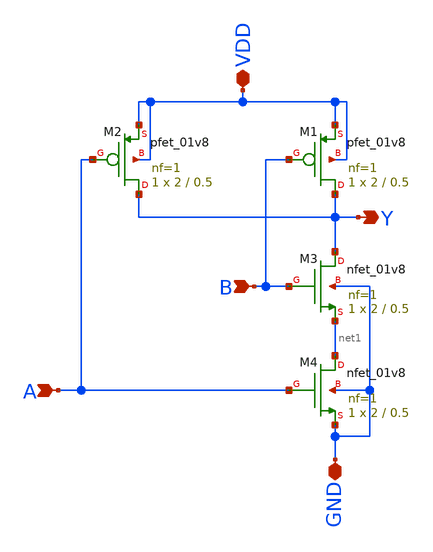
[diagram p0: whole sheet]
** sch_path: NAND.sch
**.subckt NAND A B VDD GND Y
*.ipin A
*.ipin B
*.iopin VDD
*.iopin GND
*.opin Y
XM1 Y B VDD VDD sky130_fd_pr__pfet_01v8 L=0.5 W=2 nf=1 ad='int((nf+1)/2) * W/nf * 0.29' as='int((nf+2)/2) * W/nf * 0.29'
+ pd='2*int((nf+1)/2) * (W/nf + 0.29)' ps='2*int((nf+2)/2) * (W/nf + 0.29)' nrd='0.29 / W' nrs='0.29 / W'
+ sa=0 sb=0 sd=0 mult=1 m=1
XM2 Y A VDD VDD sky130_fd_pr__pfet_01v8 L=0.5 W=2 nf=1 ad='int((nf+1)/2) * W/nf * 0.29' as='int((nf+2)/2) * W/nf * 0.29'
+ pd='2*int((nf+1)/2) * (W/nf + 0.29)' ps='2*int((nf+2)/2) * (W/nf + 0.29)' nrd='0.29 / W' nrs='0.29 / W'
+ sa=0 sb=0 sd=0 mult=1 m=1
XM3 Y B net1 GND sky130_fd_pr__nfet_01v8 L=0.5 W=2 nf=1 ad='int((nf+1)/2) * W/nf * 0.29' as='int((nf+2)/2) * W/nf * 0.29'
+ pd='2*int((nf+1)/2) * (W/nf + 0.29)' ps='2*int((nf+2)/2) * (W/nf + 0.29)' nrd='0.29 / W' nrs='0.29 / W'
+ sa=0 sb=0 sd=0 mult=1 m=1
XM4 net1 A GND GND sky130_fd_pr__nfet_01v8 L=0.5 W=2 nf=1 ad='int((nf+1)/2) * W/nf * 0.29' as='int((nf+2)/2) * W/nf * 0.29'
+ pd='2*int((nf+1)/2) * (W/nf + 0.29)' ps='2*int((nf+2)/2) * (W/nf + 0.29)' nrd='0.29 / W' nrs='0.29 / W'
+ sa=0 sb=0 sd=0 mult=1 m=1
**.ends
.end
